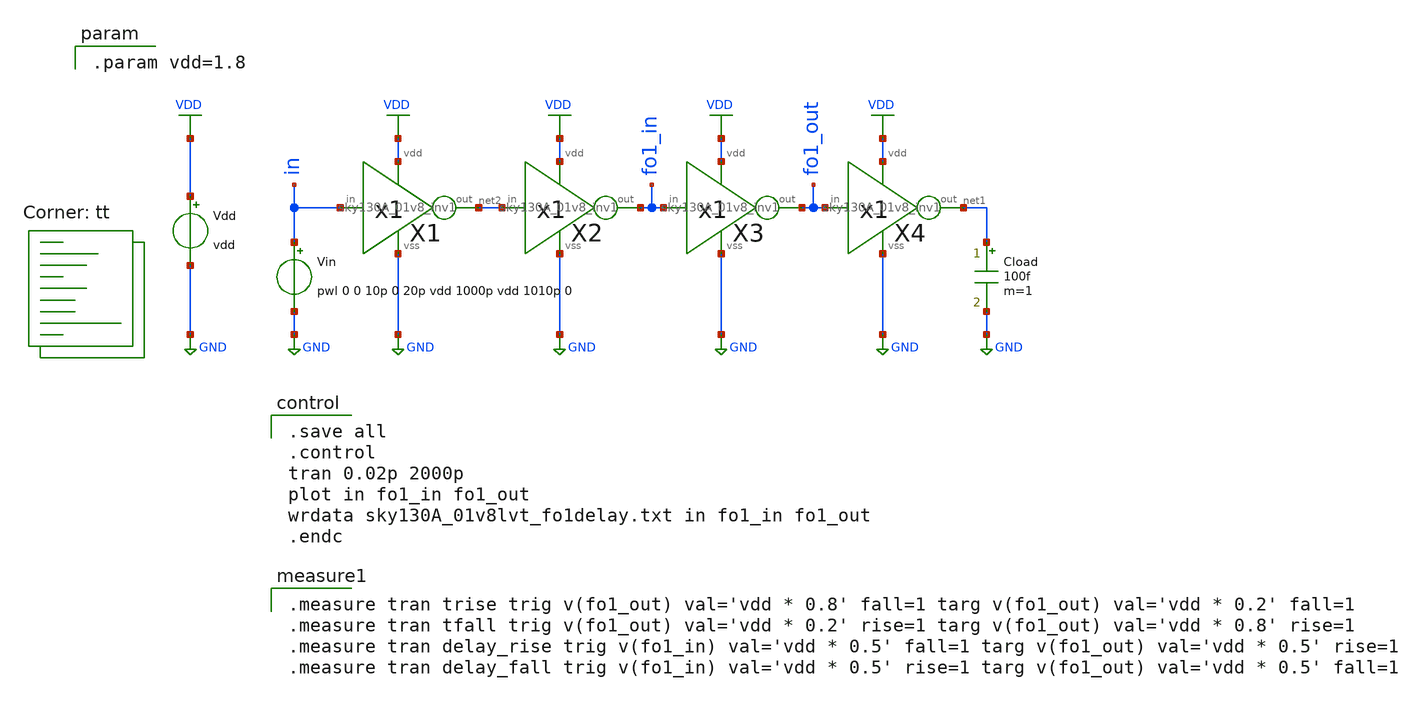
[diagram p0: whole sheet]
** sch_path: xschem/Logic/sky130A_01v8_fo1delay.sch
* Copyright 2021 Stefan Frederik Schippers
* Licensed under the Apache License, Version 2.0 (the "License");
* you may not use this file except in compliance with the License.
* You may obtain a copy of the License at
* https://www.apache.org/licenses/LICENSE-2.0
* Unless required by applicable law or agreed to in writing, software
* distributed under the License is distributed on an "AS IS" BASIS,
* WITHOUT WARRANTIES OR CONDITIONS OF ANY KIND, either express or implied.
* See the License for the specific language governing permissions and
* limitations under the License.
**.subckt sky130A_01v8_fo1delay
Vdd VDD GND vdd
Vin in GND pwl 0 0 10p 0 20p vdd 1000p vdd 1010p 0
Cload net1 GND 100f m=1
X1 VDD GND net2 in sky130A_01v8_inv1
X2 VDD GND fo1_in net2 sky130A_01v8_inv1
X3 VDD GND fo1_out fo1_in sky130A_01v8_inv1
X4 VDD GND net1 fo1_out sky130A_01v8_inv1
**** begin user architecture code

.save all
.control
tran 0.02p 2000p
plot in fo1_in fo1_out
wrdata sky130A_01v8lvt_fo1delay.txt in fo1_in fo1_out
.endc

.lib $::SKYWATER_MODELS/sky130.lib.spice tt

.measure tran trise trig v(fo1_out) val='vdd * 0.8' fall=1 targ v(fo1_out) val='vdd * 0.2' fall=1
.measure tran tfall trig v(fo1_out) val='vdd * 0.2' rise=1 targ v(fo1_out) val='vdd * 0.8' rise=1
.measure tran delay_rise trig v(fo1_in) val='vdd * 0.5' fall=1 targ v(fo1_out) val='vdd * 0.5' rise=1
.measure tran delay_fall trig v(fo1_in) val='vdd * 0.5' rise=1 targ v(fo1_out) val='vdd * 0.5' fall=1


.param vdd=1.8

**** end user architecture code
**.ends

* expanding   symbol:  symbols/sky130A_01v8_inv1.sym # of pins=4
** sym_path: xschem/symbols/sky130A_01v8_inv1.sym
** sch_path: xschem/symbols/sky130A_01v8_inv1.sch
.subckt sky130A_01v8_inv1 vdd vss out in
*.iopin vdd
*.iopin vss
*.ipin in
*.opin out
XM11 out in vdd vdd sky130_fd_pr__pfet_01v8 L=0.15 W=2 nf=1 ad='int((nf+1)/2) * W/nf * 0.29' as='int((nf+2)/2) * W/nf * 0.29'
+ pd='2*int((nf+1)/2) * (W/nf + 0.29)' ps='2*int((nf+2)/2) * (W/nf + 0.29)' nrd='0.29 / W' nrs='0.29 / W'
+ sa=0 sb=0 sd=0 mult=1 m=1
XM2 out in vss vss sky130_fd_pr__nfet_01v8 L=0.15 W=1 nf=1 ad='int((1 + 1)/2) * 1 / 1 * 0.29' as='int((1 + 2)/2) * 1 / 1 * 0.29'
+ pd='2*int((1 + 1)/2) * (1 / 1 + 0.29)' ps='2*int((1 + 2)/2) * (1 / 1 + 0.29)' nrd='0.29 / 1 ' nrs='0.29 / 1 '
+ sa=0 sb=0 sd=0 mult=1 m=1
.ends

.GLOBAL VDD
.GLOBAL GND
.end
